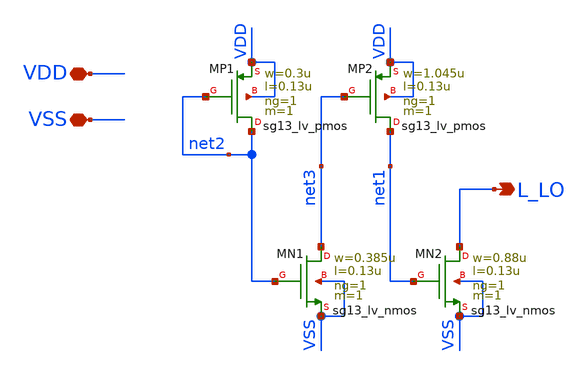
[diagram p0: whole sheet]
** sch_path: xschem/sg13g2_tielo.sch
**.subckt sg13g2_tielo VSS VDD L_LO
*.iopin VSS
*.iopin VDD
*.opin L_LO
XMN1 net3 net2 VSS VSS sg13_lv_nmos w=0.385u l=0.13u ng=1 m=1 mm_ok=1
XMP1 net2 net2 VDD VDD sg13_lv_pmos w=0.3u l=0.13u ng=1 m=1 mm_ok=1
XMN2 L_LO net1 VSS VSS sg13_lv_nmos w=0.88u l=0.13u ng=1 m=1 mm_ok=1
XMP2 net1 net3 VDD VDD sg13_lv_pmos w=1.045u l=0.13u ng=1 m=1 mm_ok=1
**.ends
.end
